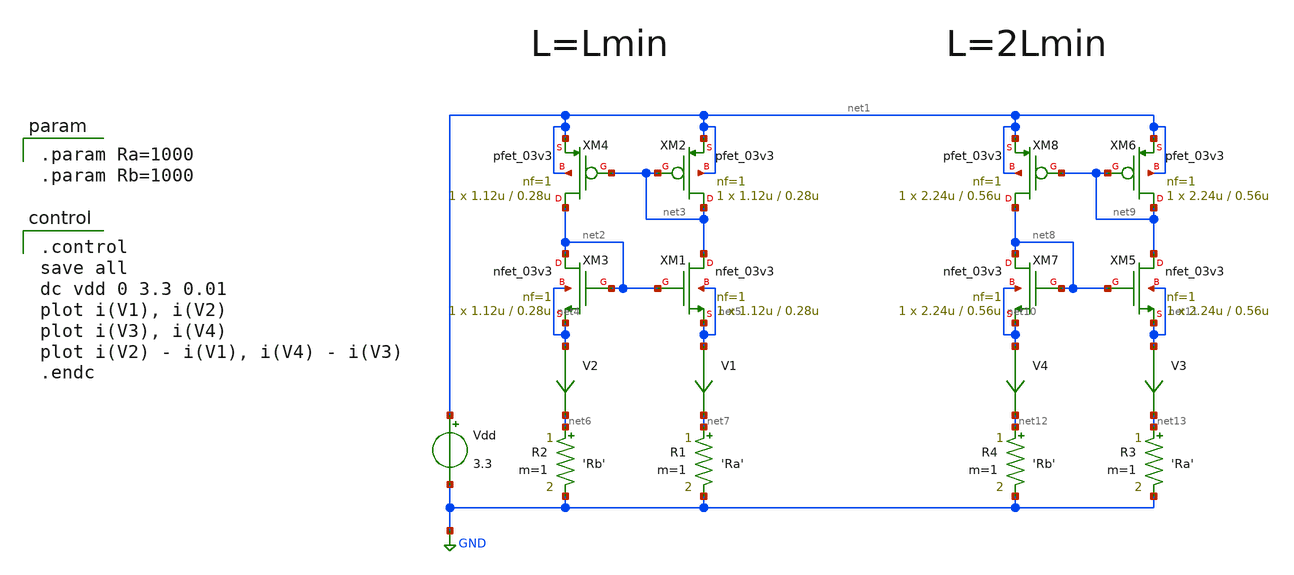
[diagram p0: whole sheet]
** sch_path: bgr/self-bias-currentmirror.sch
**.subckt self-bias-currentmirror
Vdd net1 GND 3.3
XM1 net3 net2 net5 net5 nfet_03v3 L=0.28u W=1.12u nf=1 ad='int((nf+1)/2) * W/nf * 0.18u' as='int((nf+2)/2) * W/nf * 0.18u'
+ pd='2*int((nf+1)/2) * (W/nf + 0.18u)' ps='2*int((nf+2)/2) * (W/nf + 0.18u)' nrd='0.18u / W' nrs='0.18u / W'
+ sa=0 sb=0 sd=0 m=1
XM2 net3 net3 net1 net1 pfet_03v3 L=0.28u W=1.12u nf=1 ad='int((nf+1)/2) * W/nf * 0.18u' as='int((nf+2)/2) * W/nf * 0.18u'
+ pd='2*int((nf+1)/2) * (W/nf + 0.18u)' ps='2*int((nf+2)/2) * (W/nf + 0.18u)' nrd='0.18u / W' nrs='0.18u / W'
+ sa=0 sb=0 sd=0 m=1
XM3 net2 net2 net4 net4 nfet_03v3 L=0.28u W=1.12u nf=1 ad='int((nf+1)/2) * W/nf * 0.18u' as='int((nf+2)/2) * W/nf * 0.18u'
+ pd='2*int((nf+1)/2) * (W/nf + 0.18u)' ps='2*int((nf+2)/2) * (W/nf + 0.18u)' nrd='0.18u / W' nrs='0.18u / W'
+ sa=0 sb=0 sd=0 m=1
XM4 net2 net3 net1 net1 pfet_03v3 L=0.28u W=1.12u nf=1 ad='int((nf+1)/2) * W/nf * 0.18u' as='int((nf+2)/2) * W/nf * 0.18u'
+ pd='2*int((nf+1)/2) * (W/nf + 0.18u)' ps='2*int((nf+2)/2) * (W/nf + 0.18u)' nrd='0.18u / W' nrs='0.18u / W'
+ sa=0 sb=0 sd=0 m=1
V2 net4 net6 0
.save i(v2)
V1 net5 net7 0
.save i(v1)
R1 net7 GND 'Ra' m=1
XM5 net9 net8 net11 net11 nfet_03v3 L=0.56u W=2.24u nf=1 ad='int((nf+1)/2) * W/nf * 0.18u' as='int((nf+2)/2) * W/nf * 0.18u'
+ pd='2*int((nf+1)/2) * (W/nf + 0.18u)' ps='2*int((nf+2)/2) * (W/nf + 0.18u)' nrd='0.18u / W' nrs='0.18u / W'
+ sa=0 sb=0 sd=0 m=1
XM6 net9 net9 net1 net1 pfet_03v3 L=0.56u W=2.24u nf=1 ad='int((nf+1)/2) * W/nf * 0.18u' as='int((nf+2)/2) * W/nf * 0.18u'
+ pd='2*int((nf+1)/2) * (W/nf + 0.18u)' ps='2*int((nf+2)/2) * (W/nf + 0.18u)' nrd='0.18u / W' nrs='0.18u / W'
+ sa=0 sb=0 sd=0 m=1
XM7 net8 net8 net10 net10 nfet_03v3 L=0.56u W=2.24u nf=1 ad='int((nf+1)/2) * W/nf * 0.18u' as='int((nf+2)/2) * W/nf * 0.18u'
+ pd='2*int((nf+1)/2) * (W/nf + 0.18u)' ps='2*int((nf+2)/2) * (W/nf + 0.18u)' nrd='0.18u / W' nrs='0.18u / W'
+ sa=0 sb=0 sd=0 m=1
XM8 net8 net9 net1 net1 pfet_03v3 L=0.56u W=2.24u nf=1 ad='int((nf+1)/2) * W/nf * 0.18u' as='int((nf+2)/2) * W/nf * 0.18u'
+ pd='2*int((nf+1)/2) * (W/nf + 0.18u)' ps='2*int((nf+2)/2) * (W/nf + 0.18u)' nrd='0.18u / W' nrs='0.18u / W'
+ sa=0 sb=0 sd=0 m=1
V3 net11 net13 0
.save i(v3)
V4 net10 net12 0
.save i(v4)
R3 net13 GND 'Ra' m=1
R2 net6 GND 'Rb' m=1
R4 net12 GND 'Rb' m=1
**** begin user architecture code

.include $::180MCU_MODELS/design.ngspice
.lib $::180MCU_MODELS/sm141064.ngspice typical
.lib $::180MCU_MODELS/sm141064.ngspice res_typical
.lib $::180MCU_MODELS/sm141064.ngspice moscap_typical
.lib $::180MCU_MODELS/sm141064.ngspice bjt_typical
* .lib $::180MCU_MODELS/sm141064.ngspice res_statistical


.control
save all
dc vdd 0 3.3 0.01
plot i(V1), i(V2)
plot i(V3), i(V4)
plot i(V2) - i(V1), i(V4) - i(V3)
.endc


.param Ra=1000
.param Rb=1000

**** end user architecture code
**.ends
.GLOBAL GND
.end
